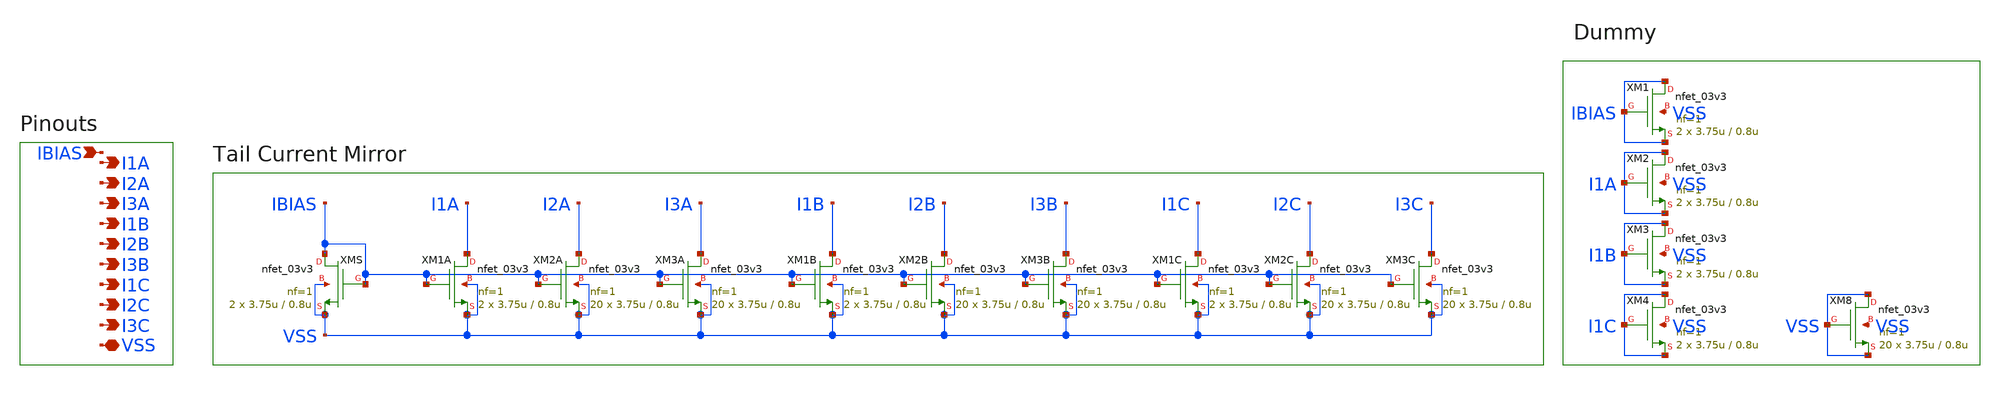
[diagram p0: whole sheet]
** sch_path: designs/libs/core_ota/tail_current_diff_out/tail_current_diff_out.sch
**.subckt tail_current_diff_out IBIAS VSS I1A I2A I1B I2B I1C I2C I3A I3B I3C
*.ipin IBIAS
*.iopin VSS
*.opin I1A
*.opin I2A
*.opin I1B
*.opin I2B
*.opin I1C
*.opin I2C
*.opin I3A
*.opin I3B
*.opin I3C
XM1A I1A IBIAS VSS VSS nfet_03v3 L=0.8u W=3.75u nf=1 ad='int((nf+1)/2) * W/nf * 0.18u' as='int((nf+2)/2) * W/nf * 0.18u'
+ pd='2*int((nf+1)/2) * (W/nf + 0.18u)' ps='2*int((nf+2)/2) * (W/nf + 0.18u)' nrd='0.18u / W' nrs='0.18u / W'
+ sa=0 sb=0 sd=0 m=2
XM2A I2A IBIAS VSS VSS nfet_03v3 L=0.8u W=3.75u nf=1 ad='int((nf+1)/2) * W/nf * 0.18u' as='int((nf+2)/2) * W/nf * 0.18u'
+ pd='2*int((nf+1)/2) * (W/nf + 0.18u)' ps='2*int((nf+2)/2) * (W/nf + 0.18u)' nrd='0.18u / W' nrs='0.18u / W'
+ sa=0 sb=0 sd=0 m=20
XM1B I1B IBIAS VSS VSS nfet_03v3 L=0.8u W=3.75u nf=1 ad='int((nf+1)/2) * W/nf * 0.18u' as='int((nf+2)/2) * W/nf * 0.18u'
+ pd='2*int((nf+1)/2) * (W/nf + 0.18u)' ps='2*int((nf+2)/2) * (W/nf + 0.18u)' nrd='0.18u / W' nrs='0.18u / W'
+ sa=0 sb=0 sd=0 m=2
XM2B I2B IBIAS VSS VSS nfet_03v3 L=0.8u W=3.75u nf=1 ad='int((nf+1)/2) * W/nf * 0.18u' as='int((nf+2)/2) * W/nf * 0.18u'
+ pd='2*int((nf+1)/2) * (W/nf + 0.18u)' ps='2*int((nf+2)/2) * (W/nf + 0.18u)' nrd='0.18u / W' nrs='0.18u / W'
+ sa=0 sb=0 sd=0 m=20
XM1C I1C IBIAS VSS VSS nfet_03v3 L=0.8u W=3.75u nf=1 ad='int((nf+1)/2) * W/nf * 0.18u' as='int((nf+2)/2) * W/nf * 0.18u'
+ pd='2*int((nf+1)/2) * (W/nf + 0.18u)' ps='2*int((nf+2)/2) * (W/nf + 0.18u)' nrd='0.18u / W' nrs='0.18u / W'
+ sa=0 sb=0 sd=0 m=2
XM2C I2C IBIAS VSS VSS nfet_03v3 L=0.8u W=3.75u nf=1 ad='int((nf+1)/2) * W/nf * 0.18u' as='int((nf+2)/2) * W/nf * 0.18u'
+ pd='2*int((nf+1)/2) * (W/nf + 0.18u)' ps='2*int((nf+2)/2) * (W/nf + 0.18u)' nrd='0.18u / W' nrs='0.18u / W'
+ sa=0 sb=0 sd=0 m=20
XMS IBIAS IBIAS VSS VSS nfet_03v3 L=0.8u W=3.75u nf=1 ad='int((nf+1)/2) * W/nf * 0.18u' as='int((nf+2)/2) * W/nf * 0.18u'
+ pd='2*int((nf+1)/2) * (W/nf + 0.18u)' ps='2*int((nf+2)/2) * (W/nf + 0.18u)' nrd='0.18u / W' nrs='0.18u / W'
+ sa=0 sb=0 sd=0 m=2
XM1 IBIAS IBIAS IBIAS VSS nfet_03v3 L=0.8u W=3.75u nf=1 ad='int((nf+1)/2) * W/nf * 0.18u' as='int((nf+2)/2) * W/nf * 0.18u'
+ pd='2*int((nf+1)/2) * (W/nf + 0.18u)' ps='2*int((nf+2)/2) * (W/nf + 0.18u)' nrd='0.18u / W' nrs='0.18u / W'
+ sa=0 sb=0 sd=0 m=2
XM2 I1A I1A I1A VSS nfet_03v3 L=0.8u W=3.75u nf=1 ad='int((nf+1)/2) * W/nf * 0.18u' as='int((nf+2)/2) * W/nf * 0.18u'
+ pd='2*int((nf+1)/2) * (W/nf + 0.18u)' ps='2*int((nf+2)/2) * (W/nf + 0.18u)' nrd='0.18u / W' nrs='0.18u / W'
+ sa=0 sb=0 sd=0 m=2
XM3 I1B I1B I1B VSS nfet_03v3 L=0.8u W=3.75u nf=1 ad='int((nf+1)/2) * W/nf * 0.18u' as='int((nf+2)/2) * W/nf * 0.18u'
+ pd='2*int((nf+1)/2) * (W/nf + 0.18u)' ps='2*int((nf+2)/2) * (W/nf + 0.18u)' nrd='0.18u / W' nrs='0.18u / W'
+ sa=0 sb=0 sd=0 m=2
XM4 I1C I1C I1C VSS nfet_03v3 L=0.8u W=3.75u nf=1 ad='int((nf+1)/2) * W/nf * 0.18u' as='int((nf+2)/2) * W/nf * 0.18u'
+ pd='2*int((nf+1)/2) * (W/nf + 0.18u)' ps='2*int((nf+2)/2) * (W/nf + 0.18u)' nrd='0.18u / W' nrs='0.18u / W'
+ sa=0 sb=0 sd=0 m=2
XM8 VSS VSS VSS VSS nfet_03v3 L=0.8u W=3.75u nf=1 ad='int((nf+1)/2) * W/nf * 0.18u' as='int((nf+2)/2) * W/nf * 0.18u'
+ pd='2*int((nf+1)/2) * (W/nf + 0.18u)' ps='2*int((nf+2)/2) * (W/nf + 0.18u)' nrd='0.18u / W' nrs='0.18u / W'
+ sa=0 sb=0 sd=0 m=20
XM3A I3A IBIAS VSS VSS nfet_03v3 L=0.8u W=3.75u nf=1 ad='int((nf+1)/2) * W/nf * 0.18u' as='int((nf+2)/2) * W/nf * 0.18u'
+ pd='2*int((nf+1)/2) * (W/nf + 0.18u)' ps='2*int((nf+2)/2) * (W/nf + 0.18u)' nrd='0.18u / W' nrs='0.18u / W'
+ sa=0 sb=0 sd=0 m=20
XM3B I3B IBIAS VSS VSS nfet_03v3 L=0.8u W=3.75u nf=1 ad='int((nf+1)/2) * W/nf * 0.18u' as='int((nf+2)/2) * W/nf * 0.18u'
+ pd='2*int((nf+1)/2) * (W/nf + 0.18u)' ps='2*int((nf+2)/2) * (W/nf + 0.18u)' nrd='0.18u / W' nrs='0.18u / W'
+ sa=0 sb=0 sd=0 m=20
XM3C I3C IBIAS VSS VSS nfet_03v3 L=0.8u W=3.75u nf=1 ad='int((nf+1)/2) * W/nf * 0.18u' as='int((nf+2)/2) * W/nf * 0.18u'
+ pd='2*int((nf+1)/2) * (W/nf + 0.18u)' ps='2*int((nf+2)/2) * (W/nf + 0.18u)' nrd='0.18u / W' nrs='0.18u / W'
+ sa=0 sb=0 sd=0 m=20
**.ends
.end
